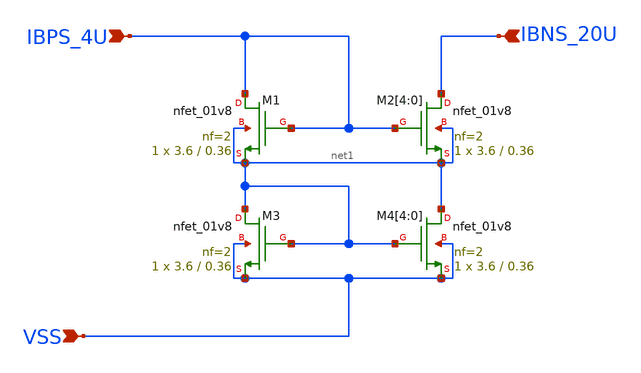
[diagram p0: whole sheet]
** sch_path: design/RPLY_EX0_SKY130NM/RPLY_EX0.sch
**.subckt RPLY_EX0 VSS IBNS_20U IBPS_4U
*.ipin VSS
*.ipin IBNS_20U
*.ipin IBPS_4U
XM1 IBPS_4U IBPS_4U net1 net1 sky130_fd_pr__nfet_01v8 L=0.36 W=3.6 nf=2 ad='int((nf+1)/2) * W/nf * 0.29'
+ as='int((nf+2)/2) * W/nf * 0.29' pd='2*int((nf+1)/2) * (W/nf + 0.29)' ps='2*int((nf+2)/2) * (W/nf + 0.29)'
+ nrd='0.29 / W' nrs='0.29 / W' sa=0 sb=0 sd=0 mult=1 m=1
XM2[4] IBNS_20U IBPS_4U net1 net1 sky130_fd_pr__nfet_01v8 L=0.36 W=3.6 nf=2 ad='int((nf+1)/2) * W/nf * 0.29'
+ as='int((nf+2)/2) * W/nf * 0.29' pd='2*int((nf+1)/2) * (W/nf + 0.29)' ps='2*int((nf+2)/2) * (W/nf + 0.29)'
+ nrd='0.29 / W' nrs='0.29 / W' sa=0 sb=0 sd=0 mult=1 m=1
XM2[3] IBNS_20U IBPS_4U net1 net1 sky130_fd_pr__nfet_01v8 L=0.36 W=3.6 nf=2 ad='int((nf+1)/2) * W/nf * 0.29'
+ as='int((nf+2)/2) * W/nf * 0.29' pd='2*int((nf+1)/2) * (W/nf + 0.29)' ps='2*int((nf+2)/2) * (W/nf + 0.29)'
+ nrd='0.29 / W' nrs='0.29 / W' sa=0 sb=0 sd=0 mult=1 m=1
XM2[2] IBNS_20U IBPS_4U net1 net1 sky130_fd_pr__nfet_01v8 L=0.36 W=3.6 nf=2 ad='int((nf+1)/2) * W/nf * 0.29'
+ as='int((nf+2)/2) * W/nf * 0.29' pd='2*int((nf+1)/2) * (W/nf + 0.29)' ps='2*int((nf+2)/2) * (W/nf + 0.29)'
+ nrd='0.29 / W' nrs='0.29 / W' sa=0 sb=0 sd=0 mult=1 m=1
XM2[1] IBNS_20U IBPS_4U net1 net1 sky130_fd_pr__nfet_01v8 L=0.36 W=3.6 nf=2 ad='int((nf+1)/2) * W/nf * 0.29'
+ as='int((nf+2)/2) * W/nf * 0.29' pd='2*int((nf+1)/2) * (W/nf + 0.29)' ps='2*int((nf+2)/2) * (W/nf + 0.29)'
+ nrd='0.29 / W' nrs='0.29 / W' sa=0 sb=0 sd=0 mult=1 m=1
XM2[0] IBNS_20U IBPS_4U net1 net1 sky130_fd_pr__nfet_01v8 L=0.36 W=3.6 nf=2 ad='int((nf+1)/2) * W/nf * 0.29'
+ as='int((nf+2)/2) * W/nf * 0.29' pd='2*int((nf+1)/2) * (W/nf + 0.29)' ps='2*int((nf+2)/2) * (W/nf + 0.29)'
+ nrd='0.29 / W' nrs='0.29 / W' sa=0 sb=0 sd=0 mult=1 m=1
XM3 net1 net1 VSS VSS sky130_fd_pr__nfet_01v8 L=0.36 W=3.6 nf=2 ad='int((nf+1)/2) * W/nf * 0.29' as='int((nf+2)/2) * W/nf * 0.29'
+ pd='2*int((nf+1)/2) * (W/nf + 0.29)' ps='2*int((nf+2)/2) * (W/nf + 0.29)' nrd='0.29 / W' nrs='0.29 / W'
+ sa=0 sb=0 sd=0 mult=1 m=1
XM4[4] net1 net1 VSS VSS sky130_fd_pr__nfet_01v8 L=0.36 W=3.6 nf=2 ad='int((nf+1)/2) * W/nf * 0.29' as='int((nf+2)/2) * W/nf * 0.29'
+ pd='2*int((nf+1)/2) * (W/nf + 0.29)' ps='2*int((nf+2)/2) * (W/nf + 0.29)' nrd='0.29 / W' nrs='0.29 / W'
+ sa=0 sb=0 sd=0 mult=1 m=1
XM4[3] net1 net1 VSS VSS sky130_fd_pr__nfet_01v8 L=0.36 W=3.6 nf=2 ad='int((nf+1)/2) * W/nf * 0.29' as='int((nf+2)/2) * W/nf * 0.29'
+ pd='2*int((nf+1)/2) * (W/nf + 0.29)' ps='2*int((nf+2)/2) * (W/nf + 0.29)' nrd='0.29 / W' nrs='0.29 / W'
+ sa=0 sb=0 sd=0 mult=1 m=1
XM4[2] net1 net1 VSS VSS sky130_fd_pr__nfet_01v8 L=0.36 W=3.6 nf=2 ad='int((nf+1)/2) * W/nf * 0.29' as='int((nf+2)/2) * W/nf * 0.29'
+ pd='2*int((nf+1)/2) * (W/nf + 0.29)' ps='2*int((nf+2)/2) * (W/nf + 0.29)' nrd='0.29 / W' nrs='0.29 / W'
+ sa=0 sb=0 sd=0 mult=1 m=1
XM4[1] net1 net1 VSS VSS sky130_fd_pr__nfet_01v8 L=0.36 W=3.6 nf=2 ad='int((nf+1)/2) * W/nf * 0.29' as='int((nf+2)/2) * W/nf * 0.29'
+ pd='2*int((nf+1)/2) * (W/nf + 0.29)' ps='2*int((nf+2)/2) * (W/nf + 0.29)' nrd='0.29 / W' nrs='0.29 / W'
+ sa=0 sb=0 sd=0 mult=1 m=1
XM4[0] net1 net1 VSS VSS sky130_fd_pr__nfet_01v8 L=0.36 W=3.6 nf=2 ad='int((nf+1)/2) * W/nf * 0.29' as='int((nf+2)/2) * W/nf * 0.29'
+ pd='2*int((nf+1)/2) * (W/nf + 0.29)' ps='2*int((nf+2)/2) * (W/nf + 0.29)' nrd='0.29 / W' nrs='0.29 / W'
+ sa=0 sb=0 sd=0 mult=1 m=1
**.ends
.end
